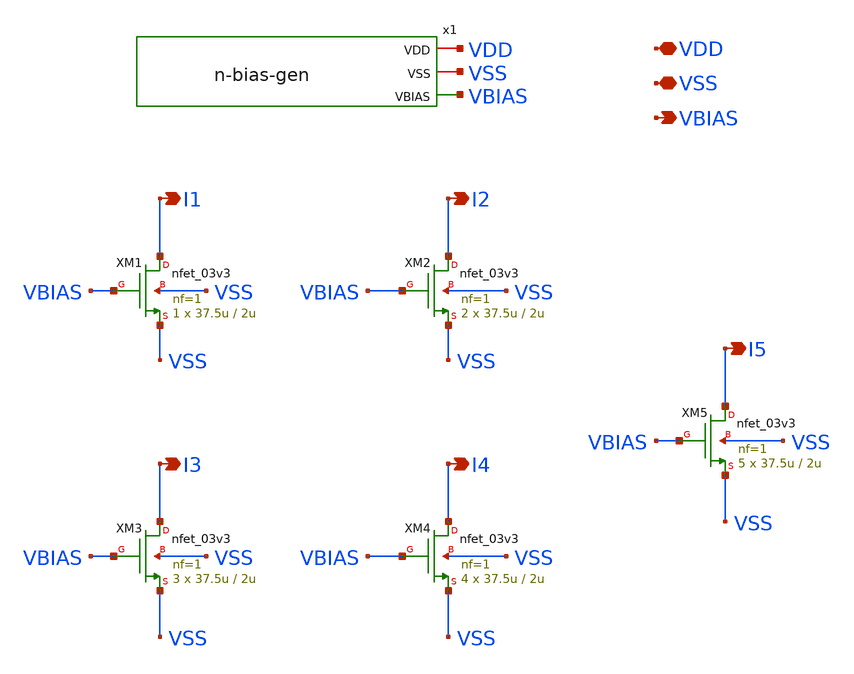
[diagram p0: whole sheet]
** sch_path: w1_advanced-foundation/w1_task/w1_current_mirror/nmos-current-mirror.sch
**.subckt nmos-current-mirror I4 I3 I1 I2 I5 VDD VSS VBIAS
*.opin I4
*.opin I3
*.opin I1
*.opin I2
*.opin I5
*.iopin VDD
*.iopin VSS
*.opin VBIAS
XM1 I1 VBIAS VSS VSS nfet_03v3 L=2u W=37.5u nf=1 ad='int((nf+1)/2) * W/nf * 0.18u' as='int((nf+2)/2) * W/nf * 0.18u'
+ pd='2*int((nf+1)/2) * (W/nf + 0.18u)' ps='2*int((nf+2)/2) * (W/nf + 0.18u)' nrd='0.18u / W' nrs='0.18u / W'
+ sa=0 sb=0 sd=0 m=1
XM2 I2 VBIAS VSS VSS nfet_03v3 L=2u W=37.5u nf=1 ad='int((nf+1)/2) * W/nf * 0.18u' as='int((nf+2)/2) * W/nf * 0.18u'
+ pd='2*int((nf+1)/2) * (W/nf + 0.18u)' ps='2*int((nf+2)/2) * (W/nf + 0.18u)' nrd='0.18u / W' nrs='0.18u / W'
+ sa=0 sb=0 sd=0 m=2
XM3 I3 VBIAS VSS VSS nfet_03v3 L=2u W=37.5u nf=1 ad='int((nf+1)/2) * W/nf * 0.18u' as='int((nf+2)/2) * W/nf * 0.18u'
+ pd='2*int((nf+1)/2) * (W/nf + 0.18u)' ps='2*int((nf+2)/2) * (W/nf + 0.18u)' nrd='0.18u / W' nrs='0.18u / W'
+ sa=0 sb=0 sd=0 m=3
XM4 I4 VBIAS VSS VSS nfet_03v3 L=2u W=37.5u nf=1 ad='int((nf+1)/2) * W/nf * 0.18u' as='int((nf+2)/2) * W/nf * 0.18u'
+ pd='2*int((nf+1)/2) * (W/nf + 0.18u)' ps='2*int((nf+2)/2) * (W/nf + 0.18u)' nrd='0.18u / W' nrs='0.18u / W'
+ sa=0 sb=0 sd=0 m=4
XM5 I5 VBIAS VSS VSS nfet_03v3 L=2u W=37.5u nf=1 ad='int((nf+1)/2) * W/nf * 0.18u' as='int((nf+2)/2) * W/nf * 0.18u'
+ pd='2*int((nf+1)/2) * (W/nf + 0.18u)' ps='2*int((nf+2)/2) * (W/nf + 0.18u)' nrd='0.18u / W' nrs='0.18u / W'
+ sa=0 sb=0 sd=0 m=5
x1 VDD VSS VBIAS n-bias-gen
**.ends

* expanding   symbol:
*+  /foss/designs/aic-sems-v/w1_advanced-foundation/w1_task/w1_current_mirror/n-bias-gen.sym # of pins=3
** sym_path: w1_advanced-foundation/w1_task/w1_current_mirror/n-bias-gen.sym
** sch_path: w1_advanced-foundation/w1_task/w1_current_mirror/n-bias-gen.sch
.subckt n-bias-gen VDD VSS VBIAS
*.iopin VDD
*.iopin VSS
*.opin VBIAS
XM1 VBIAS VBIAS VSS VSS nfet_03v3 L=2u W=37.5u nf=1 ad='int((nf+1)/2) * W/nf * 0.18u' as='int((nf+2)/2) * W/nf * 0.18u'
+ pd='2*int((nf+1)/2) * (W/nf + 0.18u)' ps='2*int((nf+2)/2) * (W/nf + 0.18u)' nrd='0.18u / W' nrs='0.18u / W'
+ sa=0 sb=0 sd=0 m=1
XR1 VBIAS net9 VSS ppolyf_u_1k r_width=4e-6 r_length=100e-6 m=1
XR2 net1 VDD VSS ppolyf_u_1k r_width=4e-6 r_length=100e-6 m=1
XR3 net2 net1 VSS ppolyf_u_1k r_width=4e-6 r_length=100e-6 m=1
XR4 net9 net8 VSS ppolyf_u_1k r_width=4e-6 r_length=100e-6 m=1
XR5 net3 net2 VSS ppolyf_u_1k r_width=4e-6 r_length=100e-6 m=1
XR6 net8 net7 VSS ppolyf_u_1k r_width=4e-6 r_length=100e-6 m=1
XR7 net4 net3 VSS ppolyf_u_1k r_width=4e-6 r_length=100e-6 m=1
XR8 net7 net6 VSS ppolyf_u_1k r_width=4e-6 r_length=100e-6 m=1
XR9 net5 net4 VSS ppolyf_u_1k r_width=4e-6 r_length=100e-6 m=1
XR10 net6 net5 VSS ppolyf_u_1k r_width=4e-6 r_length=100e-6 m=1
.ends

.end
